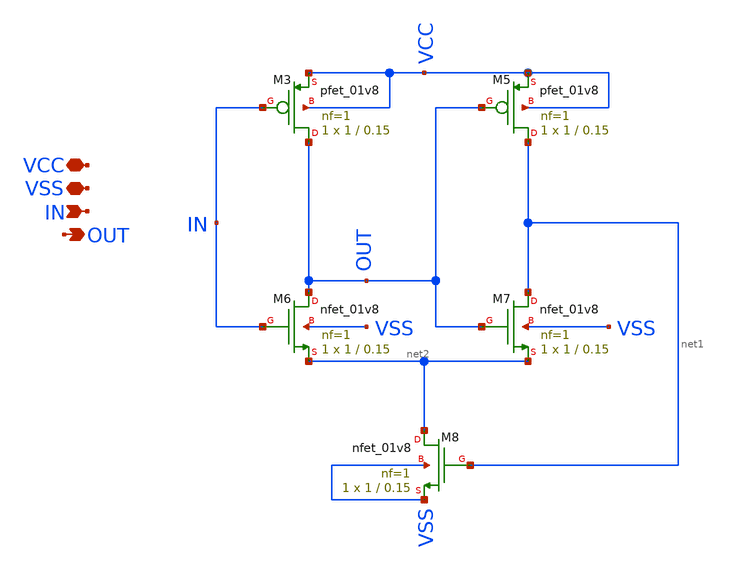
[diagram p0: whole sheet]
** sch_path: xschem/st.sch
**.subckt st VCC VSS IN OUT
*.iopin VCC
*.iopin VSS
*.ipin IN
*.opin OUT
XM3 OUT IN VCC VCC sky130_fd_pr__pfet_01v8 L=0.15 W=1 nf=1 ad='int((nf+1)/2) * W/nf * 0.29' as='int((nf+2)/2) * W/nf * 0.29'
+ pd='2*int((nf+1)/2) * (W/nf + 0.29)' ps='2*int((nf+2)/2) * (W/nf + 0.29)' nrd='0.29 / W' nrs='0.29 / W'
+ sa=0 sb=0 sd=0 mult=1 m=1
XM5 net1 OUT VCC VCC sky130_fd_pr__pfet_01v8 L=0.15 W=1 nf=1 ad='int((nf+1)/2) * W/nf * 0.29' as='int((nf+2)/2) * W/nf * 0.29'
+ pd='2*int((nf+1)/2) * (W/nf + 0.29)' ps='2*int((nf+2)/2) * (W/nf + 0.29)' nrd='0.29 / W' nrs='0.29 / W'
+ sa=0 sb=0 sd=0 mult=1 m=1
XM6 OUT IN net2 VSS sky130_fd_pr__nfet_01v8 L=0.15 W=1 nf=1 ad='int((nf+1)/2) * W/nf * 0.29' as='int((nf+2)/2) * W/nf * 0.29'
+ pd='2*int((nf+1)/2) * (W/nf + 0.29)' ps='2*int((nf+2)/2) * (W/nf + 0.29)' nrd='0.29 / W' nrs='0.29 / W'
+ sa=0 sb=0 sd=0 mult=1 m=1
XM7 net1 OUT net2 VSS sky130_fd_pr__nfet_01v8 L=0.15 W=1 nf=1 ad='int((nf+1)/2) * W/nf * 0.29' as='int((nf+2)/2) * W/nf * 0.29'
+ pd='2*int((nf+1)/2) * (W/nf + 0.29)' ps='2*int((nf+2)/2) * (W/nf + 0.29)' nrd='0.29 / W' nrs='0.29 / W'
+ sa=0 sb=0 sd=0 mult=1 m=1
XM8 net2 net1 VSS VSS sky130_fd_pr__nfet_01v8 L=0.15 W=1 nf=1 ad='int((nf+1)/2) * W/nf * 0.29' as='int((nf+2)/2) * W/nf * 0.29'
+ pd='2*int((nf+1)/2) * (W/nf + 0.29)' ps='2*int((nf+2)/2) * (W/nf + 0.29)' nrd='0.29 / W' nrs='0.29 / W'
+ sa=0 sb=0 sd=0 mult=1 m=1
**.ends
.end
